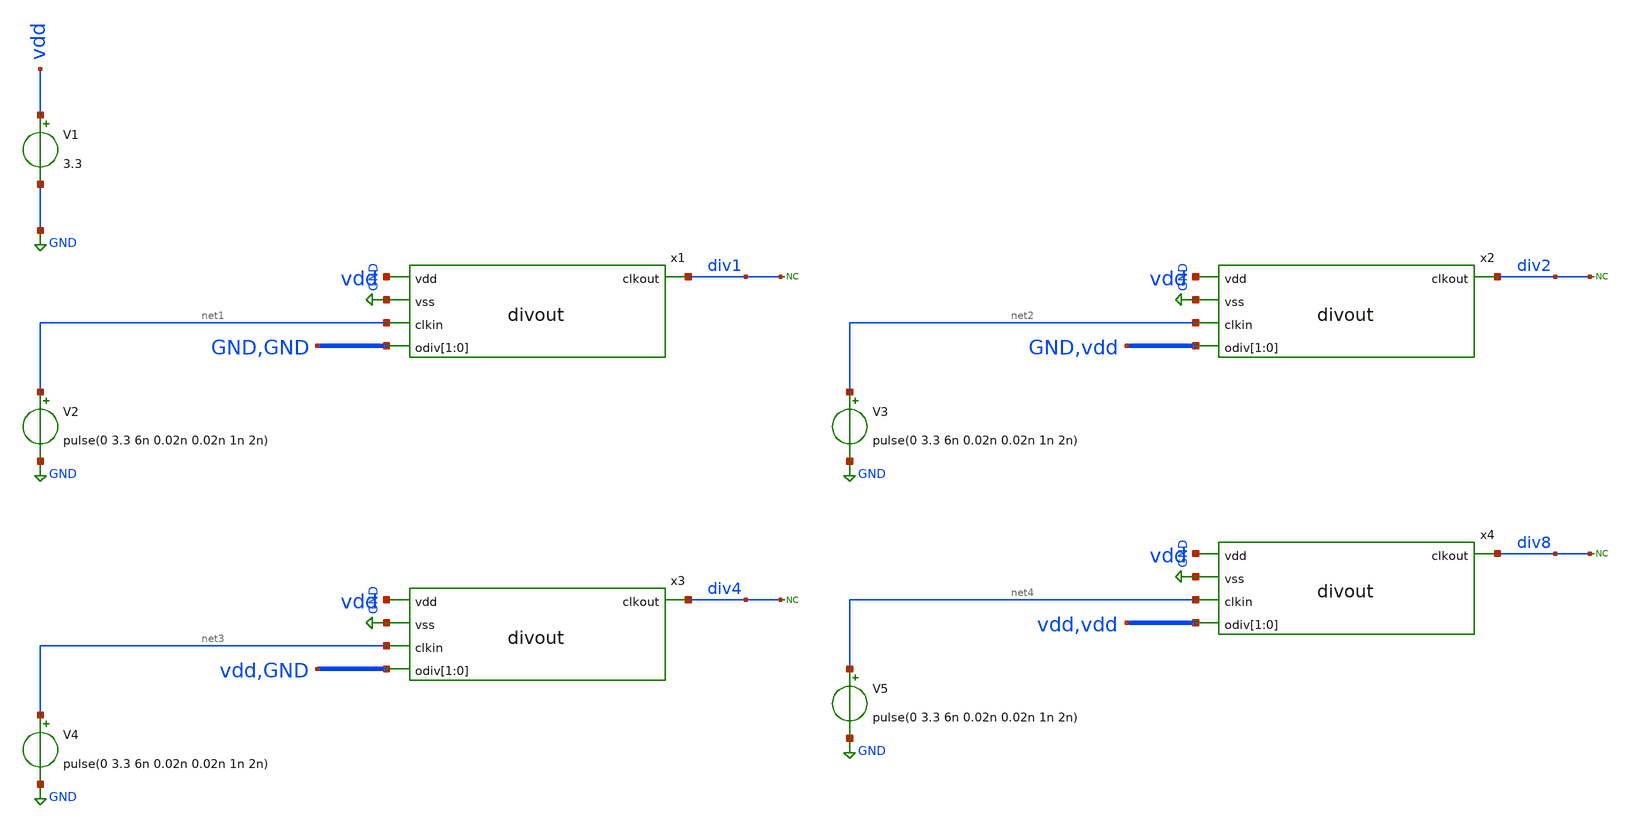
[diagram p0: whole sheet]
** sch_path: xschem/tb_divout.sch
**.subckt tb_divout
x1 vdd GND div1 net1 GND GND divout
V2 net1 GND pulse(0 3.3 6n 0.02n 0.02n 1n 2n)
V1 vdd GND 3.3
* noconn div1
x2 vdd GND div2 net2 GND vdd divout
* noconn div2
x3 vdd GND div4 net3 vdd GND divout
* noconn div4
x4 vdd GND div8 net4 vdd vdd divout
* noconn div8
V3 net2 GND pulse(0 3.3 6n 0.02n 0.02n 1n 2n)
V4 net3 GND pulse(0 3.3 6n 0.02n 0.02n 1n 2n)
V5 net4 GND pulse(0 3.3 6n 0.02n 0.02n 1n 2n)
**** begin user architecture code


.include /usr/local/share/pdk/gf180mcuD/libs.tech/ngspice/design.ngspice
.lib /usr/local/share/pdk/gf180mcuD/libs.tech/ngspice/sm141064.ngspice ss
.option temp=110

.control
save all
tran 2p 100n
run
plot div1 div2+3.3 div4+6.6 div8+9.9
plot i(V1)
.endc


**** end user architecture code
**.ends

* expanding   symbol:  divout.sym # of pins=5
** sym_path: xschem/divout.sym
** sch_path: xschem/divout.sch
.subckt divout vdd vss clkout clkin odiv[1] odiv[0]
*.ipin odiv[1],odiv[0]
*.ipin clkin
*.opin clkout
*.ipin vdd
*.ipin vss
x1 vdd sel0 div2 clkin net1 vss imux2
x3 div2 div2 vdd vss clkin dff_dynamic
x4 vdd odiv[1] div4 net1 net2 vss imux2
x5 div4 div4 vdd vss net1 dff_dynamic
x2 vdd sel2 div8 net2 clkout vss imux2
x6 div8 div8 vdd vss net2 dff_dynamic
x7 vdd odiv[1] odiv[0] sel2 vss and2
x8 vdd odiv[1] odiv[0] sel0 vss or2
.ends


* expanding   symbol:  imux2.sym # of pins=6
** sym_path: xschem/imux2.sym
** sch_path: xschem/imux2.sch
.subckt imux2 vdd sel b a outb vss
*.ipin b
*.ipin a
*.ipin sel
*.ipin vdd
*.ipin vss
*.opin outb
XM1 net2 b vdd vdd pfet_03v3 L=0.28u W=8u nf=1 ad='int((nf+1)/2) * W/nf * 0.18u' as='int((nf+2)/2) * W/nf * 0.18u'
+ pd='2*int((nf+1)/2) * (W/nf + 0.18u)' ps='2*int((nf+2)/2) * (W/nf + 0.18u)' nrd='0.18u / W' nrs='0.18u / W'
+ sa=0 sb=0 sd=0 m=1
XM2 net1 b vss vss nfet_03v3 L=0.28u W=4u nf=1 ad='int((nf+1)/2) * W/nf * 0.18u' as='int((nf+2)/2) * W/nf * 0.18u'
+ pd='2*int((nf+1)/2) * (W/nf + 0.18u)' ps='2*int((nf+2)/2) * (W/nf + 0.18u)' nrd='0.18u / W' nrs='0.18u / W'
+ sa=0 sb=0 sd=0 m=1
XM3 outb sel net1 vss nfet_03v3 L=0.28u W=4u nf=1 ad='int((nf+1)/2) * W/nf * 0.18u' as='int((nf+2)/2) * W/nf * 0.18u'
+ pd='2*int((nf+1)/2) * (W/nf + 0.18u)' ps='2*int((nf+2)/2) * (W/nf + 0.18u)' nrd='0.18u / W' nrs='0.18u / W'
+ sa=0 sb=0 sd=0 m=1
XM4 outb selb net2 vdd pfet_03v3 L=0.28u W=8u nf=1 ad='int((nf+1)/2) * W/nf * 0.18u' as='int((nf+2)/2) * W/nf * 0.18u'
+ pd='2*int((nf+1)/2) * (W/nf + 0.18u)' ps='2*int((nf+2)/2) * (W/nf + 0.18u)' nrd='0.18u / W' nrs='0.18u / W'
+ sa=0 sb=0 sd=0 m=1
XM5 net4 a vdd vdd pfet_03v3 L=0.28u W=8u nf=1 ad='int((nf+1)/2) * W/nf * 0.18u' as='int((nf+2)/2) * W/nf * 0.18u'
+ pd='2*int((nf+1)/2) * (W/nf + 0.18u)' ps='2*int((nf+2)/2) * (W/nf + 0.18u)' nrd='0.18u / W' nrs='0.18u / W'
+ sa=0 sb=0 sd=0 m=1
XM6 net3 a vss vss nfet_03v3 L=0.28u W=4u nf=1 ad='int((nf+1)/2) * W/nf * 0.18u' as='int((nf+2)/2) * W/nf * 0.18u'
+ pd='2*int((nf+1)/2) * (W/nf + 0.18u)' ps='2*int((nf+2)/2) * (W/nf + 0.18u)' nrd='0.18u / W' nrs='0.18u / W'
+ sa=0 sb=0 sd=0 m=1
XM7 outb selb net3 vss nfet_03v3 L=0.28u W=4u nf=1 ad='int((nf+1)/2) * W/nf * 0.18u' as='int((nf+2)/2) * W/nf * 0.18u'
+ pd='2*int((nf+1)/2) * (W/nf + 0.18u)' ps='2*int((nf+2)/2) * (W/nf + 0.18u)' nrd='0.18u / W' nrs='0.18u / W'
+ sa=0 sb=0 sd=0 m=1
XM8 outb sel net4 vdd pfet_03v3 L=0.28u W=8u nf=1 ad='int((nf+1)/2) * W/nf * 0.18u' as='int((nf+2)/2) * W/nf * 0.18u'
+ pd='2*int((nf+1)/2) * (W/nf + 0.18u)' ps='2*int((nf+2)/2) * (W/nf + 0.18u)' nrd='0.18u / W' nrs='0.18u / W'
+ sa=0 sb=0 sd=0 m=1
XM9 selb sel vdd vdd pfet_03v3 L=0.28u W=8u nf=1 ad='int((nf+1)/2) * W/nf * 0.18u' as='int((nf+2)/2) * W/nf * 0.18u'
+ pd='2*int((nf+1)/2) * (W/nf + 0.18u)' ps='2*int((nf+2)/2) * (W/nf + 0.18u)' nrd='0.18u / W' nrs='0.18u / W'
+ sa=0 sb=0 sd=0 m=1
XM10 selb sel vss vss nfet_03v3 L=0.28u W=4u nf=1 ad='int((nf+1)/2) * W/nf * 0.18u' as='int((nf+2)/2) * W/nf * 0.18u'
+ pd='2*int((nf+1)/2) * (W/nf + 0.18u)' ps='2*int((nf+2)/2) * (W/nf + 0.18u)' nrd='0.18u / W' nrs='0.18u / W'
+ sa=0 sb=0 sd=0 m=1
.ends


* expanding   symbol:  dff_dynamic.sym # of pins=5
** sym_path: xschem/dff_dynamic.sym
** sch_path: xschem/dff_dynamic.sch
.subckt dff_dynamic qb d vdd vss clk
*.ipin d
*.ipin vdd
*.ipin vss
*.ipin clk
*.opin qb
XM1 net1 d vss vss nfet_03v3 L=0.28u W=1u nf=1 ad='int((nf+1)/2) * W/nf * 0.18u' as='int((nf+2)/2) * W/nf * 0.18u'
+ pd='2*int((nf+1)/2) * (W/nf + 0.18u)' ps='2*int((nf+2)/2) * (W/nf + 0.18u)' nrd='0.18u / W' nrs='0.18u / W'
+ sa=0 sb=0 sd=0 m=1
XM2 net1 d vdd vdd pfet_03v3 L=0.28u W=2u nf=1 ad='int((nf+1)/2) * W/nf * 0.18u' as='int((nf+2)/2) * W/nf * 0.18u'
+ pd='2*int((nf+1)/2) * (W/nf + 0.18u)' ps='2*int((nf+2)/2) * (W/nf + 0.18u)' nrd='0.18u / W' nrs='0.18u / W'
+ sa=0 sb=0 sd=0 m=1
XM3 net1 clkb net2 vss nfet_03v3 L=0.28u W=1u nf=1 ad='int((nf+1)/2) * W/nf * 0.18u' as='int((nf+2)/2) * W/nf * 0.18u'
+ pd='2*int((nf+1)/2) * (W/nf + 0.18u)' ps='2*int((nf+2)/2) * (W/nf + 0.18u)' nrd='0.18u / W' nrs='0.18u / W'
+ sa=0 sb=0 sd=0 m=1
XM4 net1 clk net2 vdd pfet_03v3 L=0.28u W=2u nf=1 ad='int((nf+1)/2) * W/nf * 0.18u' as='int((nf+2)/2) * W/nf * 0.18u'
+ pd='2*int((nf+1)/2) * (W/nf + 0.18u)' ps='2*int((nf+2)/2) * (W/nf + 0.18u)' nrd='0.18u / W' nrs='0.18u / W'
+ sa=0 sb=0 sd=0 m=1
XM5 net3 net2 vss vss nfet_03v3 L=0.28u W=1u nf=1 ad='int((nf+1)/2) * W/nf * 0.18u' as='int((nf+2)/2) * W/nf * 0.18u'
+ pd='2*int((nf+1)/2) * (W/nf + 0.18u)' ps='2*int((nf+2)/2) * (W/nf + 0.18u)' nrd='0.18u / W' nrs='0.18u / W'
+ sa=0 sb=0 sd=0 m=1
XM6 net3 net2 vdd vdd pfet_03v3 L=0.28u W=2u nf=1 ad='int((nf+1)/2) * W/nf * 0.18u' as='int((nf+2)/2) * W/nf * 0.18u'
+ pd='2*int((nf+1)/2) * (W/nf + 0.18u)' ps='2*int((nf+2)/2) * (W/nf + 0.18u)' nrd='0.18u / W' nrs='0.18u / W'
+ sa=0 sb=0 sd=0 m=1
XM7 net4 clk net3 vss nfet_03v3 L=0.28u W=1u nf=1 ad='int((nf+1)/2) * W/nf * 0.18u' as='int((nf+2)/2) * W/nf * 0.18u'
+ pd='2*int((nf+1)/2) * (W/nf + 0.18u)' ps='2*int((nf+2)/2) * (W/nf + 0.18u)' nrd='0.18u / W' nrs='0.18u / W'
+ sa=0 sb=0 sd=0 m=1
XM8 net4 clkb net3 vdd pfet_03v3 L=0.28u W=2u nf=1 ad='int((nf+1)/2) * W/nf * 0.18u' as='int((nf+2)/2) * W/nf * 0.18u'
+ pd='2*int((nf+1)/2) * (W/nf + 0.18u)' ps='2*int((nf+2)/2) * (W/nf + 0.18u)' nrd='0.18u / W' nrs='0.18u / W'
+ sa=0 sb=0 sd=0 m=1
XM9 qb net4 vss vss nfet_03v3 L=0.28u W=1u nf=1 ad='int((nf+1)/2) * W/nf * 0.18u' as='int((nf+2)/2) * W/nf * 0.18u'
+ pd='2*int((nf+1)/2) * (W/nf + 0.18u)' ps='2*int((nf+2)/2) * (W/nf + 0.18u)' nrd='0.18u / W' nrs='0.18u / W'
+ sa=0 sb=0 sd=0 m=1
XM10 qb net4 vdd vdd pfet_03v3 L=0.28u W=2u nf=1 ad='int((nf+1)/2) * W/nf * 0.18u' as='int((nf+2)/2) * W/nf * 0.18u'
+ pd='2*int((nf+1)/2) * (W/nf + 0.18u)' ps='2*int((nf+2)/2) * (W/nf + 0.18u)' nrd='0.18u / W' nrs='0.18u / W'
+ sa=0 sb=0 sd=0 m=1
XM11 clkb clk vss vss nfet_03v3 L=0.28u W=1u nf=1 ad='int((nf+1)/2) * W/nf * 0.18u' as='int((nf+2)/2) * W/nf * 0.18u'
+ pd='2*int((nf+1)/2) * (W/nf + 0.18u)' ps='2*int((nf+2)/2) * (W/nf + 0.18u)' nrd='0.18u / W' nrs='0.18u / W'
+ sa=0 sb=0 sd=0 m=1
XM12 clkb clk vdd vdd pfet_03v3 L=0.28u W=2u nf=1 ad='int((nf+1)/2) * W/nf * 0.18u' as='int((nf+2)/2) * W/nf * 0.18u'
+ pd='2*int((nf+1)/2) * (W/nf + 0.18u)' ps='2*int((nf+2)/2) * (W/nf + 0.18u)' nrd='0.18u / W' nrs='0.18u / W'
+ sa=0 sb=0 sd=0 m=1
.ends


* expanding   symbol:  and2.sym # of pins=5
** sym_path: xschem/and2.sym
** sch_path: xschem/and2.sch
.subckt and2 vdd a b out vss
*.ipin a
*.ipin b
*.ipin vdd
*.ipin vss
*.opin out
XM47 net1 b net2 vss nfet_03v3 L=0.28u W=0.6u nf=1 ad='int((nf+1)/2) * W/nf * 0.18u' as='int((nf+2)/2) * W/nf * 0.18u'
+ pd='2*int((nf+1)/2) * (W/nf + 0.18u)' ps='2*int((nf+2)/2) * (W/nf + 0.18u)' nrd='0.18u / W' nrs='0.18u / W'
+ sa=0 sb=0 sd=0 m=1
XM48 net1 b vdd vdd pfet_03v3 L=0.28u W=1.2u nf=1 ad='int((nf+1)/2) * W/nf * 0.18u' as='int((nf+2)/2) * W/nf * 0.18u'
+ pd='2*int((nf+1)/2) * (W/nf + 0.18u)' ps='2*int((nf+2)/2) * (W/nf + 0.18u)' nrd='0.18u / W' nrs='0.18u / W'
+ sa=0 sb=0 sd=0 m=1
XM49 net2 a vss vss nfet_03v3 L=0.28u W=0.6u nf=1 ad='int((nf+1)/2) * W/nf * 0.18u' as='int((nf+2)/2) * W/nf * 0.18u'
+ pd='2*int((nf+1)/2) * (W/nf + 0.18u)' ps='2*int((nf+2)/2) * (W/nf + 0.18u)' nrd='0.18u / W' nrs='0.18u / W'
+ sa=0 sb=0 sd=0 m=1
XM50 net1 a vdd vdd pfet_03v3 L=0.28u W=1.2u nf=1 ad='int((nf+1)/2) * W/nf * 0.18u' as='int((nf+2)/2) * W/nf * 0.18u'
+ pd='2*int((nf+1)/2) * (W/nf + 0.18u)' ps='2*int((nf+2)/2) * (W/nf + 0.18u)' nrd='0.18u / W' nrs='0.18u / W'
+ sa=0 sb=0 sd=0 m=1
XM51 out net1 vss vss nfet_03v3 L=0.28u W=0.6u nf=1 ad='int((nf+1)/2) * W/nf * 0.18u' as='int((nf+2)/2) * W/nf * 0.18u'
+ pd='2*int((nf+1)/2) * (W/nf + 0.18u)' ps='2*int((nf+2)/2) * (W/nf + 0.18u)' nrd='0.18u / W' nrs='0.18u / W'
+ sa=0 sb=0 sd=0 m=1
XM52 out net1 vdd vdd pfet_03v3 L=0.28u W=1.2u nf=1 ad='int((nf+1)/2) * W/nf * 0.18u' as='int((nf+2)/2) * W/nf * 0.18u'
+ pd='2*int((nf+1)/2) * (W/nf + 0.18u)' ps='2*int((nf+2)/2) * (W/nf + 0.18u)' nrd='0.18u / W' nrs='0.18u / W'
+ sa=0 sb=0 sd=0 m=1
.ends


* expanding   symbol:  or2.sym # of pins=5
** sym_path: xschem/or2.sym
** sch_path: xschem/or2.sch
.subckt or2 vdd a b out vss
*.ipin a
*.ipin b
*.ipin vdd
*.ipin vss
*.opin out
XM29 net1 b vss vss nfet_03v3 L=0.28u W=0.6u nf=1 ad='int((nf+1)/2) * W/nf * 0.18u' as='int((nf+2)/2) * W/nf * 0.18u'
+ pd='2*int((nf+1)/2) * (W/nf + 0.18u)' ps='2*int((nf+2)/2) * (W/nf + 0.18u)' nrd='0.18u / W' nrs='0.18u / W'
+ sa=0 sb=0 sd=0 m=1
XM30 net2 a vdd vdd pfet_03v3 L=0.28u W=1.2u nf=1 ad='int((nf+1)/2) * W/nf * 0.18u' as='int((nf+2)/2) * W/nf * 0.18u'
+ pd='2*int((nf+1)/2) * (W/nf + 0.18u)' ps='2*int((nf+2)/2) * (W/nf + 0.18u)' nrd='0.18u / W' nrs='0.18u / W'
+ sa=0 sb=0 sd=0 m=1
XM31 net1 a vss vss nfet_03v3 L=0.28u W=0.6u nf=1 ad='int((nf+1)/2) * W/nf * 0.18u' as='int((nf+2)/2) * W/nf * 0.18u'
+ pd='2*int((nf+1)/2) * (W/nf + 0.18u)' ps='2*int((nf+2)/2) * (W/nf + 0.18u)' nrd='0.18u / W' nrs='0.18u / W'
+ sa=0 sb=0 sd=0 m=1
XM32 net1 b net2 vdd pfet_03v3 L=0.28u W=1.2u nf=1 ad='int((nf+1)/2) * W/nf * 0.18u' as='int((nf+2)/2) * W/nf * 0.18u'
+ pd='2*int((nf+1)/2) * (W/nf + 0.18u)' ps='2*int((nf+2)/2) * (W/nf + 0.18u)' nrd='0.18u / W' nrs='0.18u / W'
+ sa=0 sb=0 sd=0 m=1
XM13 out net1 vss vss nfet_03v3 L=0.28u W=0.6u nf=1 ad='int((nf+1)/2) * W/nf * 0.18u' as='int((nf+2)/2) * W/nf * 0.18u'
+ pd='2*int((nf+1)/2) * (W/nf + 0.18u)' ps='2*int((nf+2)/2) * (W/nf + 0.18u)' nrd='0.18u / W' nrs='0.18u / W'
+ sa=0 sb=0 sd=0 m=1
XM14 out net1 vdd vdd pfet_03v3 L=0.28u W=1.2u nf=1 ad='int((nf+1)/2) * W/nf * 0.18u' as='int((nf+2)/2) * W/nf * 0.18u'
+ pd='2*int((nf+1)/2) * (W/nf + 0.18u)' ps='2*int((nf+2)/2) * (W/nf + 0.18u)' nrd='0.18u / W' nrs='0.18u / W'
+ sa=0 sb=0 sd=0 m=1
.ends

.GLOBAL GND
.end
